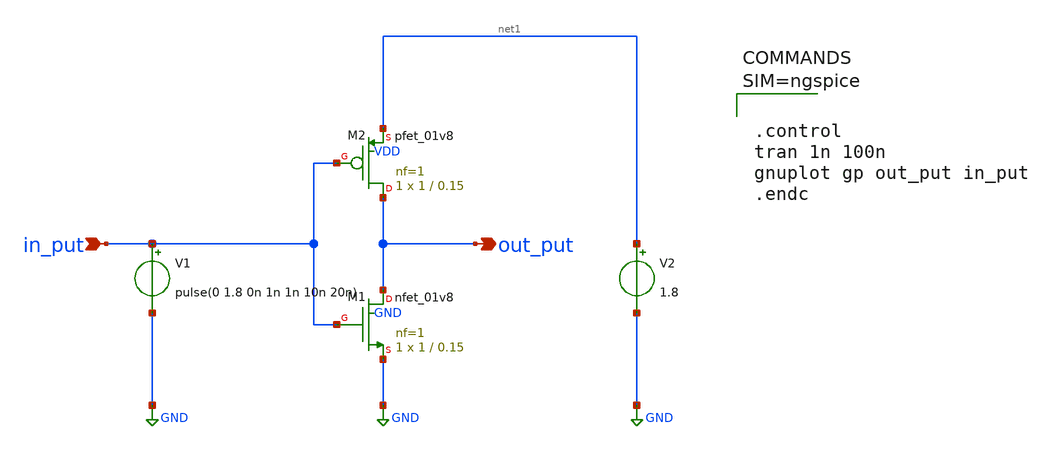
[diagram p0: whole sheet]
** sch_path: Ngspice/Inverter/CMOS_INVERTER.sch
**.subckt CMOS_INVERTER out_put in_put
*.opin out_put
*.ipin in_put
XM1 out_put in_put GND GND sky130_fd_pr__nfet_01v8 L=0.15 W=1 nf=1 ad='int((1 + 1)/2) * 1 / 1 * 0.29'
+ as='int((1 + 2)/2) * 1 / 1 * 0.29' pd='2*int((1 + 1)/2) * (1 / 1 + 0.29)' ps='2*int((1 + 2)/2) * (1 / 1 + 0.29)'
+ nrd='0.29 / 1 ' nrs='0.29 / 1 ' sa=0 sb=0 sd=0 mult=1 m=1
XM2 out_put in_put net1 VDD sky130_fd_pr__pfet_01v8 L=0.15 W=1 nf=1 ad='int((1 + 1)/2) * 1 / 1 * 0.29'
+ as='int((1 + 2)/2) * 1 / 1 * 0.29' pd='2*int((1 + 1)/2) * (1 / 1 + 0.29)' ps='2*int((1 + 2)/2) * (1 / 1 + 0.29)'
+ nrd='0.29 / 1 ' nrs='0.29 / 1 ' sa=0 sb=0 sd=0 mult=1 m=1
V1 in_put GND pulse(0 1.8 0n 1n 1n 10n 20n)
V2 net1 GND 1.8
**** begin user architecture code

** opencircuitdesign pdks install
.lib $::SKYWATER_MODELS/sky130.lib.spice tt




.control
tran 1n 100n
gnuplot gp out_put in_put
.endc



**** end user architecture code
**.ends
.GLOBAL GND
.end
